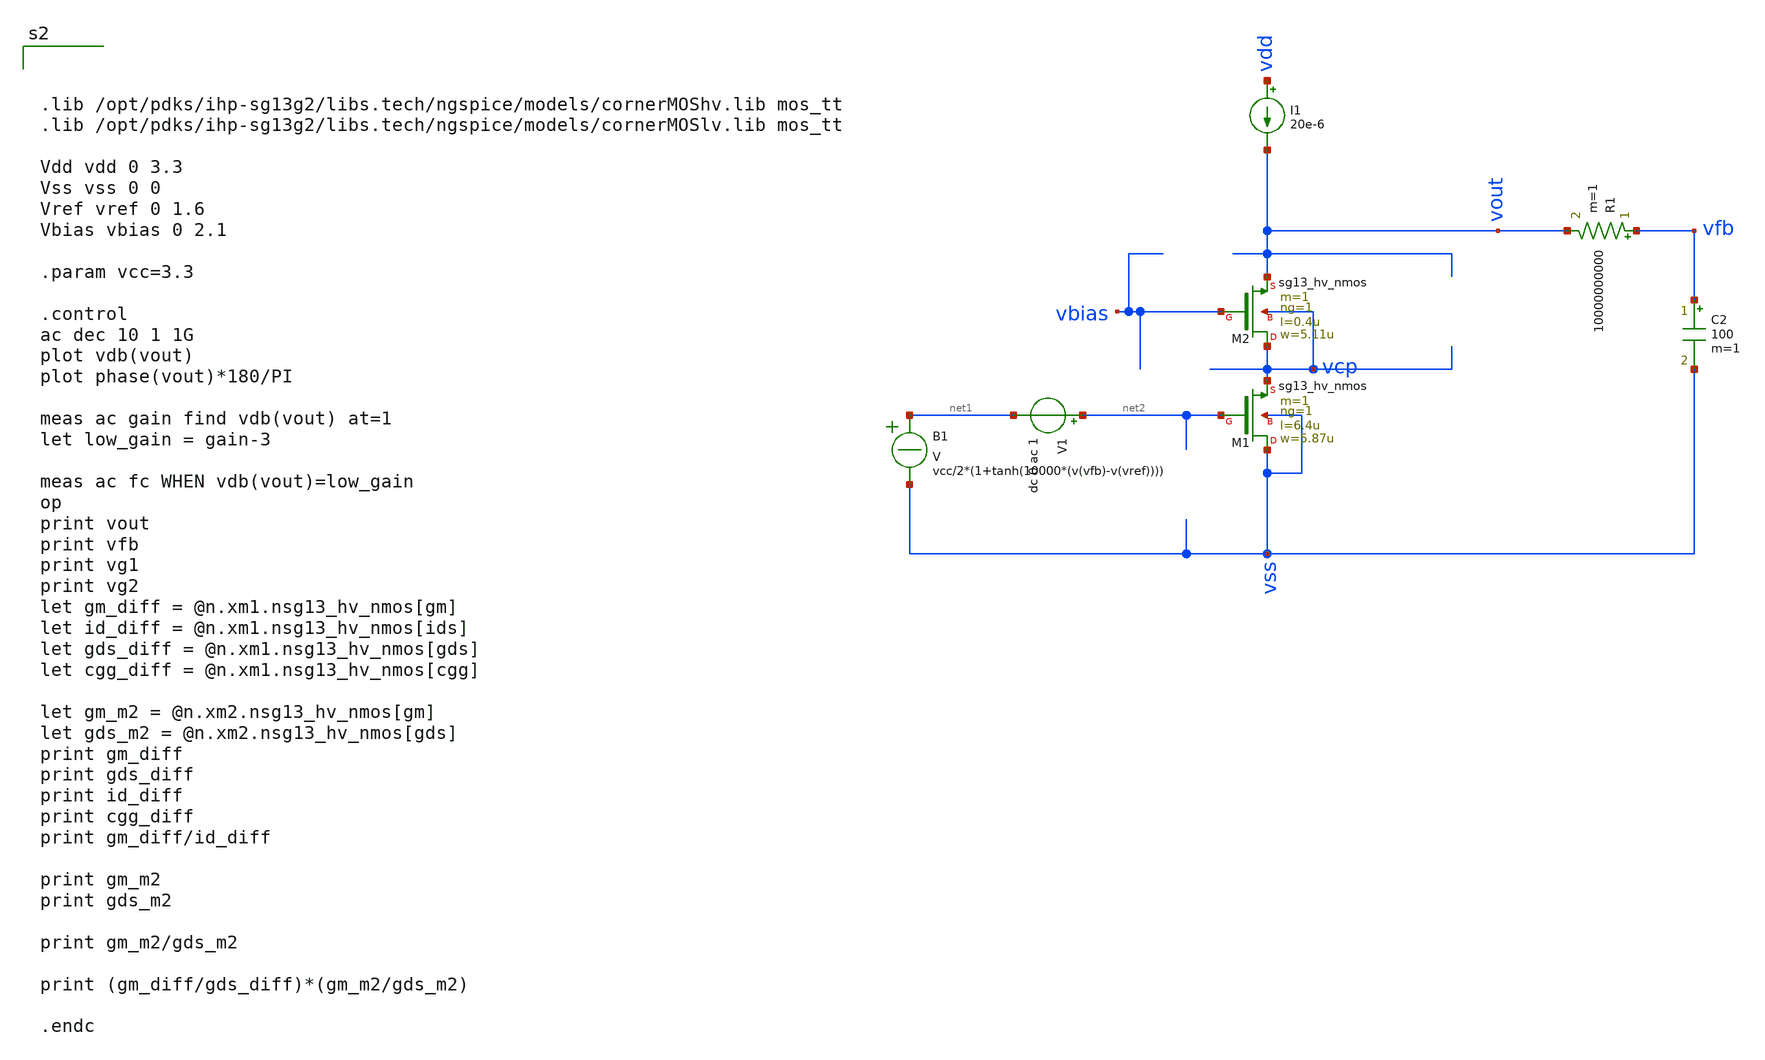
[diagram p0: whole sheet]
** sch_path: test-python/sstadex/xschem/cascode_test_full.sch
**.subckt cascode_test_full
XM1 vss net2 vcp vss sg13_hv_nmos w=5.87u l=6.4u ng=1 m=1 mm_ok=1
XM2 vcp vbias vout vcp sg13_hv_nmos w=5.11u l=0.4u ng=1 m=1 mm_ok=1
B1 net1 vss V = vcc/2*(1+tanh(10000*(v(vfb)-v(vref))))
V1 net2 net1 dc 0 ac 1
R1 vfb vout 10000000000 m=1
C2 vfb vss 100 m=1
I1 vdd vout 20e-6
**** begin user architecture code



.lib /opt/pdks/ihp-sg13g2/libs.tech/ngspice/models/cornerMOShv.lib mos_tt
.lib /opt/pdks/ihp-sg13g2/libs.tech/ngspice/models/cornerMOSlv.lib mos_tt

Vdd vdd 0 3.3
Vss vss 0 0
Vref vref 0 1.6
Vbias vbias 0 2.1

.param vcc=3.3

.control
ac dec 10 1 1G
plot vdb(vout)
plot phase(vout)*180/PI

meas ac gain find vdb(vout) at=1
let low_gain = gain-3

meas ac fc WHEN vdb(vout)=low_gain
op
print vout
print vfb
print vg1
print vg2
let gm_diff = @n.xm1.nsg13_hv_nmos[gm]
let id_diff = @n.xm1.nsg13_hv_nmos[ids]
let gds_diff = @n.xm1.nsg13_hv_nmos[gds]
let cgg_diff = @n.xm1.nsg13_hv_nmos[cgg]

let gm_m2 = @n.xm2.nsg13_hv_nmos[gm]
let gds_m2 = @n.xm2.nsg13_hv_nmos[gds]
print gm_diff
print gds_diff
print id_diff
print cgg_diff
print gm_diff/id_diff

print gm_m2
print gds_m2

print gm_m2/gds_m2

print (gm_diff/gds_diff)*(gm_m2/gds_m2)

.endc



**** end user architecture code
**.ends
.end
